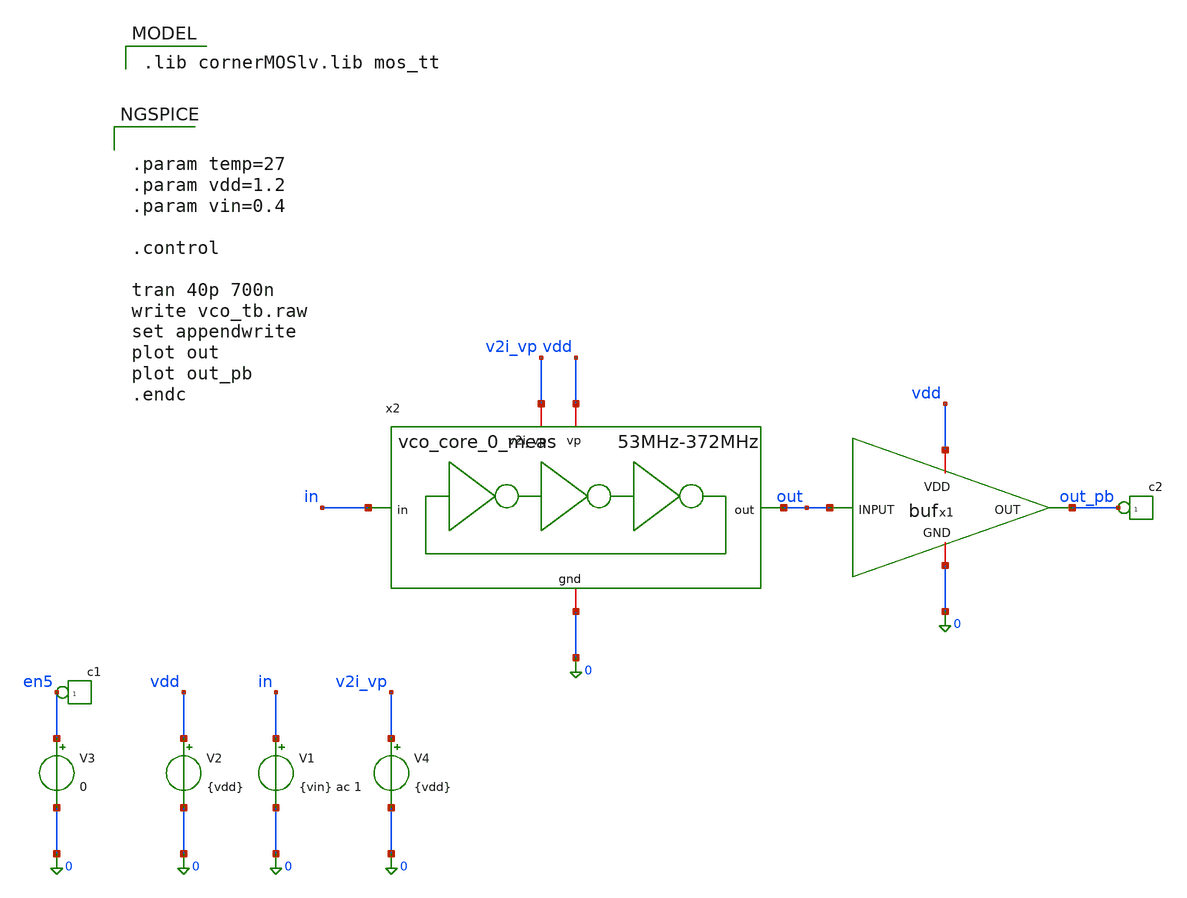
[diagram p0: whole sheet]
** sch_path: schematics/vco/vco_tb/vco_dcin_meas_tb.sch
**.subckt vco_dcin_meas_tb
V1 in 0 {vin} ac 1
.save i(v1)
V2 vdd 0 {vdd}
*connector(1,1) ?1 out_pb
x1 vdd out out_pb 0 buf
x2 vdd 0 out in v2i_vp vco_core_0_meas
V3 en5 0 0
*connector(1,1) ?1 en5
V4 v2i_vp 0 {vdd}
**** begin user architecture code


.param temp=27
.param vdd=1.2
.param vin=0.4

.control

tran 40p 700n
write vco_tb.raw
set appendwrite
plot out
plot out_pb
.endc


 .lib cornerMOSlv.lib mos_tt

**** end user architecture code
**.ends
.end
